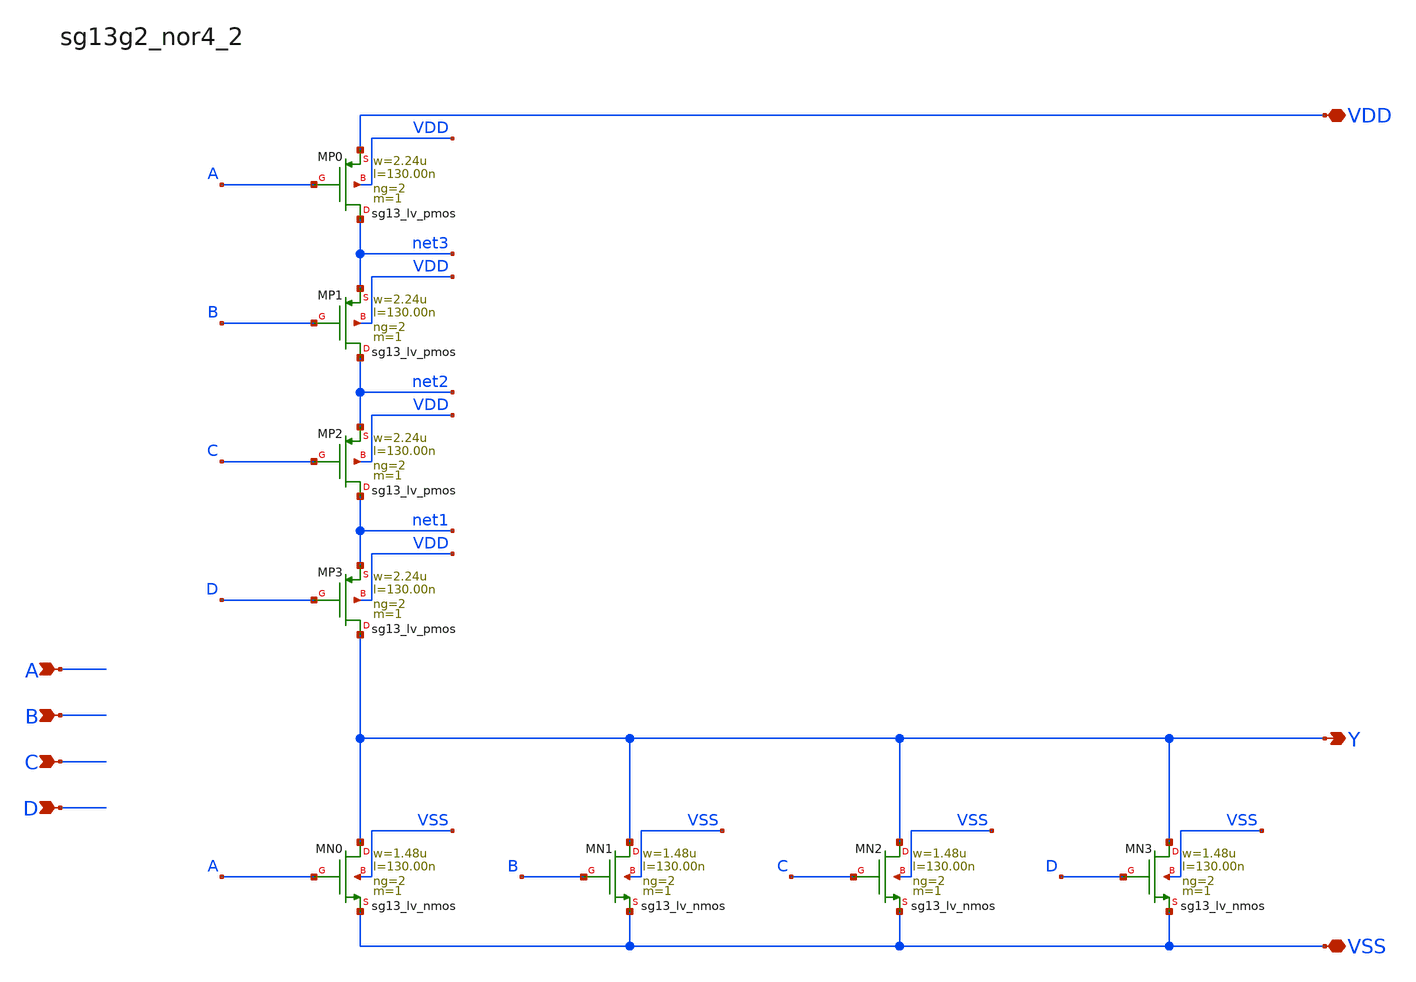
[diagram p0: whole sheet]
** sch_path: outputs/sg13g2_cells/cells/sg13g2_nor4_2/sg13g2_nor4_2.sch
**.subckt sg13g2_nor4_2 Y A B C D VDD VSS
*.opin Y
*.ipin A
*.ipin B
*.ipin C
*.ipin D
*.iopin VDD
*.iopin VSS
XMP0 net3 A VDD VDD sg13_lv_pmos w=2.24u l=130.00n ng=2 m=1 mm_ok=1
XMP1 net2 B net3 VDD sg13_lv_pmos w=2.24u l=130.00n ng=2 m=1 mm_ok=1
XMP2 net1 C net2 VDD sg13_lv_pmos w=2.24u l=130.00n ng=2 m=1 mm_ok=1
XMP3 Y D net1 VDD sg13_lv_pmos w=2.24u l=130.00n ng=2 m=1 mm_ok=1
XMN0 Y A VSS VSS sg13_lv_nmos w=1.48u l=130.00n ng=2 m=1 mm_ok=1
XMN3 Y D VSS VSS sg13_lv_nmos w=1.48u l=130.00n ng=2 m=1 mm_ok=1
XMN1 Y B VSS VSS sg13_lv_nmos w=1.48u l=130.00n ng=2 m=1 mm_ok=1
XMN2 Y C VSS VSS sg13_lv_nmos w=1.48u l=130.00n ng=2 m=1 mm_ok=1
**.ends
.end
